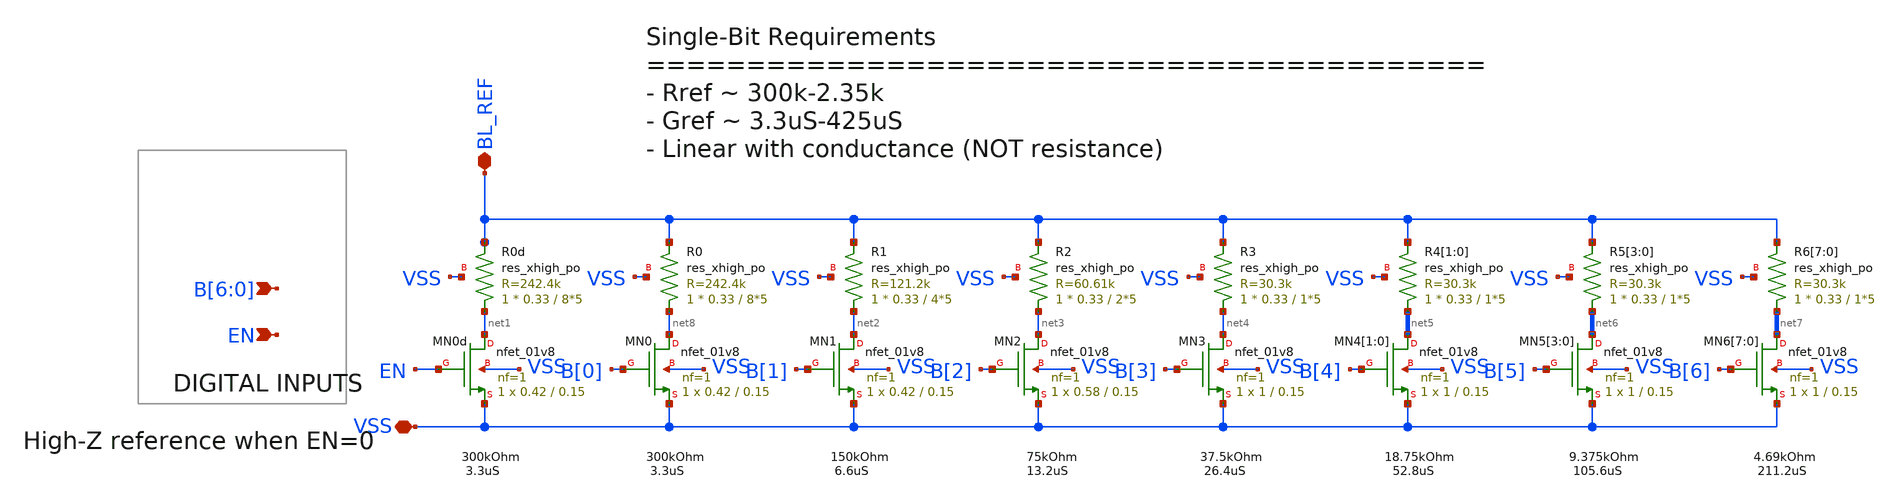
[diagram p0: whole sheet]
** sch_path: BL_Read_Interface/rram_read_csa_rref_core.sch
**.subckt rram_read_csa_rref_core VSS BL_REF B[6],B[5],B[4],B[3],B[2],B[1],B[0] EN
*.iopin VSS
*.iopin BL_REF
*.ipin B[6],B[5],B[4],B[3],B[2],B[1],B[0]
*.ipin EN
XR0d net1 BL_REF VSS sky130_fd_pr__res_xhigh_po W=0.33 L=8*5 mult=1 m=1
XR0 net8 BL_REF VSS sky130_fd_pr__res_xhigh_po W=0.33 L=8*5 mult=1 m=1
XR1 net2 BL_REF VSS sky130_fd_pr__res_xhigh_po W=0.33 L=4*5 mult=1 m=1
XR2 net3 BL_REF VSS sky130_fd_pr__res_xhigh_po W=0.33 L=2*5 mult=1 m=1
XR3 net4 BL_REF VSS sky130_fd_pr__res_xhigh_po W=0.33 L=1*5 mult=1 m=1
XR4[1] net5[1] BL_REF VSS sky130_fd_pr__res_xhigh_po W=0.33 L=1*5 mult=1 m=1
XR4[0] net5[0] BL_REF VSS sky130_fd_pr__res_xhigh_po W=0.33 L=1*5 mult=1 m=1
XR5[3] net6[3] BL_REF VSS sky130_fd_pr__res_xhigh_po W=0.33 L=1*5 mult=1 m=1
XR5[2] net6[2] BL_REF VSS sky130_fd_pr__res_xhigh_po W=0.33 L=1*5 mult=1 m=1
XR5[1] net6[1] BL_REF VSS sky130_fd_pr__res_xhigh_po W=0.33 L=1*5 mult=1 m=1
XR5[0] net6[0] BL_REF VSS sky130_fd_pr__res_xhigh_po W=0.33 L=1*5 mult=1 m=1
XR6[7] net7[7] BL_REF VSS sky130_fd_pr__res_xhigh_po W=0.33 L=1*5 mult=1 m=1
XR6[6] net7[6] BL_REF VSS sky130_fd_pr__res_xhigh_po W=0.33 L=1*5 mult=1 m=1
XR6[5] net7[5] BL_REF VSS sky130_fd_pr__res_xhigh_po W=0.33 L=1*5 mult=1 m=1
XR6[4] net7[4] BL_REF VSS sky130_fd_pr__res_xhigh_po W=0.33 L=1*5 mult=1 m=1
XR6[3] net7[3] BL_REF VSS sky130_fd_pr__res_xhigh_po W=0.33 L=1*5 mult=1 m=1
XR6[2] net7[2] BL_REF VSS sky130_fd_pr__res_xhigh_po W=0.33 L=1*5 mult=1 m=1
XR6[1] net7[1] BL_REF VSS sky130_fd_pr__res_xhigh_po W=0.33 L=1*5 mult=1 m=1
XR6[0] net7[0] BL_REF VSS sky130_fd_pr__res_xhigh_po W=0.33 L=1*5 mult=1 m=1
XMN0d net1 EN VSS VSS sky130_fd_pr__nfet_01v8 L=0.15 W=0.42 nf=1 ad='int((nf+1)/2) * W/nf * 0.29' as='int((nf+2)/2) * W/nf * 0.29'
+ pd='2*int((nf+1)/2) * (W/nf + 0.29)' ps='2*int((nf+2)/2) * (W/nf + 0.29)' nrd='0.29 / W' nrs='0.29 / W'
+ sa=0 sb=0 sd=0 mult=1 m=1
XMN0 net8 B[0] VSS VSS sky130_fd_pr__nfet_01v8 L=0.15 W=0.42 nf=1 ad='int((nf+1)/2) * W/nf * 0.29' as='int((nf+2)/2) * W/nf * 0.29'
+ pd='2*int((nf+1)/2) * (W/nf + 0.29)' ps='2*int((nf+2)/2) * (W/nf + 0.29)' nrd='0.29 / W' nrs='0.29 / W'
+ sa=0 sb=0 sd=0 mult=1 m=1
XMN1 net2 B[1] VSS VSS sky130_fd_pr__nfet_01v8 L=0.15 W=0.42 nf=1 ad='int((nf+1)/2) * W/nf * 0.29' as='int((nf+2)/2) * W/nf * 0.29'
+ pd='2*int((nf+1)/2) * (W/nf + 0.29)' ps='2*int((nf+2)/2) * (W/nf + 0.29)' nrd='0.29 / W' nrs='0.29 / W'
+ sa=0 sb=0 sd=0 mult=1 m=1
XMN2 net3 B[2] VSS VSS sky130_fd_pr__nfet_01v8 L=0.15 W=0.58 nf=1 ad='int((nf+1)/2) * W/nf * 0.29' as='int((nf+2)/2) * W/nf * 0.29'
+ pd='2*int((nf+1)/2) * (W/nf + 0.29)' ps='2*int((nf+2)/2) * (W/nf + 0.29)' nrd='0.29 / W' nrs='0.29 / W'
+ sa=0 sb=0 sd=0 mult=1 m=1
XMN3 net4 B[3] VSS VSS sky130_fd_pr__nfet_01v8 L=0.15 W=1 nf=1 ad='int((nf+1)/2) * W/nf * 0.29' as='int((nf+2)/2) * W/nf * 0.29'
+ pd='2*int((nf+1)/2) * (W/nf + 0.29)' ps='2*int((nf+2)/2) * (W/nf + 0.29)' nrd='0.29 / W' nrs='0.29 / W'
+ sa=0 sb=0 sd=0 mult=1 m=1
XMN4[1] net5[1] B[4] VSS VSS sky130_fd_pr__nfet_01v8 L=0.15 W=1 nf=1 ad='int((nf+1)/2) * W/nf * 0.29'
+ as='int((nf+2)/2) * W/nf * 0.29' pd='2*int((nf+1)/2) * (W/nf + 0.29)' ps='2*int((nf+2)/2) * (W/nf + 0.29)'
+ nrd='0.29 / W' nrs='0.29 / W' sa=0 sb=0 sd=0 mult=1 m=1
XMN4[0] net5[0] B[4] VSS VSS sky130_fd_pr__nfet_01v8 L=0.15 W=1 nf=1 ad='int((nf+1)/2) * W/nf * 0.29'
+ as='int((nf+2)/2) * W/nf * 0.29' pd='2*int((nf+1)/2) * (W/nf + 0.29)' ps='2*int((nf+2)/2) * (W/nf + 0.29)'
+ nrd='0.29 / W' nrs='0.29 / W' sa=0 sb=0 sd=0 mult=1 m=1
XMN5[3] net6[3] B[5] VSS VSS sky130_fd_pr__nfet_01v8 L=0.15 W=1 nf=1 ad='int((nf+1)/2) * W/nf * 0.29'
+ as='int((nf+2)/2) * W/nf * 0.29' pd='2*int((nf+1)/2) * (W/nf + 0.29)' ps='2*int((nf+2)/2) * (W/nf + 0.29)'
+ nrd='0.29 / W' nrs='0.29 / W' sa=0 sb=0 sd=0 mult=1 m=1
XMN5[2] net6[2] B[5] VSS VSS sky130_fd_pr__nfet_01v8 L=0.15 W=1 nf=1 ad='int((nf+1)/2) * W/nf * 0.29'
+ as='int((nf+2)/2) * W/nf * 0.29' pd='2*int((nf+1)/2) * (W/nf + 0.29)' ps='2*int((nf+2)/2) * (W/nf + 0.29)'
+ nrd='0.29 / W' nrs='0.29 / W' sa=0 sb=0 sd=0 mult=1 m=1
XMN5[1] net6[1] B[5] VSS VSS sky130_fd_pr__nfet_01v8 L=0.15 W=1 nf=1 ad='int((nf+1)/2) * W/nf * 0.29'
+ as='int((nf+2)/2) * W/nf * 0.29' pd='2*int((nf+1)/2) * (W/nf + 0.29)' ps='2*int((nf+2)/2) * (W/nf + 0.29)'
+ nrd='0.29 / W' nrs='0.29 / W' sa=0 sb=0 sd=0 mult=1 m=1
XMN5[0] net6[0] B[5] VSS VSS sky130_fd_pr__nfet_01v8 L=0.15 W=1 nf=1 ad='int((nf+1)/2) * W/nf * 0.29'
+ as='int((nf+2)/2) * W/nf * 0.29' pd='2*int((nf+1)/2) * (W/nf + 0.29)' ps='2*int((nf+2)/2) * (W/nf + 0.29)'
+ nrd='0.29 / W' nrs='0.29 / W' sa=0 sb=0 sd=0 mult=1 m=1
XMN6[7] net7[7] B[6] VSS VSS sky130_fd_pr__nfet_01v8 L=0.15 W=1 nf=1 ad='int((nf+1)/2) * W/nf * 0.29'
+ as='int((nf+2)/2) * W/nf * 0.29' pd='2*int((nf+1)/2) * (W/nf + 0.29)' ps='2*int((nf+2)/2) * (W/nf + 0.29)'
+ nrd='0.29 / W' nrs='0.29 / W' sa=0 sb=0 sd=0 mult=1 m=1
XMN6[6] net7[6] B[6] VSS VSS sky130_fd_pr__nfet_01v8 L=0.15 W=1 nf=1 ad='int((nf+1)/2) * W/nf * 0.29'
+ as='int((nf+2)/2) * W/nf * 0.29' pd='2*int((nf+1)/2) * (W/nf + 0.29)' ps='2*int((nf+2)/2) * (W/nf + 0.29)'
+ nrd='0.29 / W' nrs='0.29 / W' sa=0 sb=0 sd=0 mult=1 m=1
XMN6[5] net7[5] B[6] VSS VSS sky130_fd_pr__nfet_01v8 L=0.15 W=1 nf=1 ad='int((nf+1)/2) * W/nf * 0.29'
+ as='int((nf+2)/2) * W/nf * 0.29' pd='2*int((nf+1)/2) * (W/nf + 0.29)' ps='2*int((nf+2)/2) * (W/nf + 0.29)'
+ nrd='0.29 / W' nrs='0.29 / W' sa=0 sb=0 sd=0 mult=1 m=1
XMN6[4] net7[4] B[6] VSS VSS sky130_fd_pr__nfet_01v8 L=0.15 W=1 nf=1 ad='int((nf+1)/2) * W/nf * 0.29'
+ as='int((nf+2)/2) * W/nf * 0.29' pd='2*int((nf+1)/2) * (W/nf + 0.29)' ps='2*int((nf+2)/2) * (W/nf + 0.29)'
+ nrd='0.29 / W' nrs='0.29 / W' sa=0 sb=0 sd=0 mult=1 m=1
XMN6[3] net7[3] B[6] VSS VSS sky130_fd_pr__nfet_01v8 L=0.15 W=1 nf=1 ad='int((nf+1)/2) * W/nf * 0.29'
+ as='int((nf+2)/2) * W/nf * 0.29' pd='2*int((nf+1)/2) * (W/nf + 0.29)' ps='2*int((nf+2)/2) * (W/nf + 0.29)'
+ nrd='0.29 / W' nrs='0.29 / W' sa=0 sb=0 sd=0 mult=1 m=1
XMN6[2] net7[2] B[6] VSS VSS sky130_fd_pr__nfet_01v8 L=0.15 W=1 nf=1 ad='int((nf+1)/2) * W/nf * 0.29'
+ as='int((nf+2)/2) * W/nf * 0.29' pd='2*int((nf+1)/2) * (W/nf + 0.29)' ps='2*int((nf+2)/2) * (W/nf + 0.29)'
+ nrd='0.29 / W' nrs='0.29 / W' sa=0 sb=0 sd=0 mult=1 m=1
XMN6[1] net7[1] B[6] VSS VSS sky130_fd_pr__nfet_01v8 L=0.15 W=1 nf=1 ad='int((nf+1)/2) * W/nf * 0.29'
+ as='int((nf+2)/2) * W/nf * 0.29' pd='2*int((nf+1)/2) * (W/nf + 0.29)' ps='2*int((nf+2)/2) * (W/nf + 0.29)'
+ nrd='0.29 / W' nrs='0.29 / W' sa=0 sb=0 sd=0 mult=1 m=1
XMN6[0] net7[0] B[6] VSS VSS sky130_fd_pr__nfet_01v8 L=0.15 W=1 nf=1 ad='int((nf+1)/2) * W/nf * 0.29'
+ as='int((nf+2)/2) * W/nf * 0.29' pd='2*int((nf+1)/2) * (W/nf + 0.29)' ps='2*int((nf+2)/2) * (W/nf + 0.29)'
+ nrd='0.29 / W' nrs='0.29 / W' sa=0 sb=0 sd=0 mult=1 m=1
**.ends
.end
